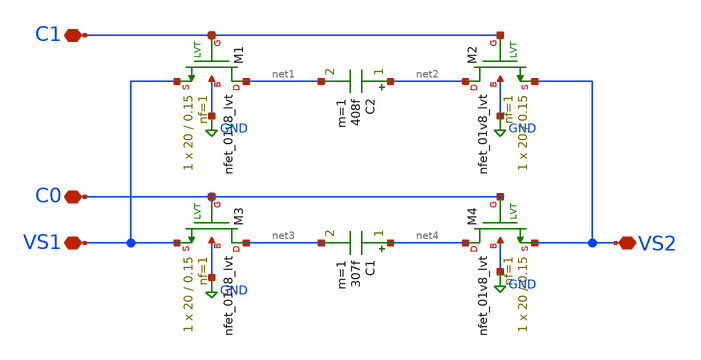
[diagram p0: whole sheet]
** sch_path: VGA/Cs_Banks.sch
**.subckt Cs_Banks VS1 VS2 C0 C1
*.iopin VS1
*.iopin VS2
*.iopin C0
*.iopin C1
XM1 net1 C1 VS1 GND sky130_fd_pr__nfet_01v8_lvt L=0.15 W=20 nf=1 ad='int((1 + 1)/2) * 20 / 1 * 0.29'
+ as='int((1 + 2)/2) * 20 / 1 * 0.29' pd='2*int((1 + 1)/2) * (20 / 1 + 0.29)' ps='2*int((1 + 2)/2) * (20 / 1 + 0.29)'
+ nrd='0.29 / 20 ' nrs='0.29 / 20 ' sa=0 sb=0 sd=0 mult=1 m=1
XM3 net3 C0 VS1 GND sky130_fd_pr__nfet_01v8_lvt L=0.15 W=20 nf=1 ad='int((1 + 1)/2) * 20 / 1 * 0.29'
+ as='int((1 + 2)/2) * 20 / 1 * 0.29' pd='2*int((1 + 1)/2) * (20 / 1 + 0.29)' ps='2*int((1 + 2)/2) * (20 / 1 + 0.29)'
+ nrd='0.29 / 20 ' nrs='0.29 / 20 ' sa=0 sb=0 sd=0 mult=1 m=1
C2 net2 net1 408f m=1
C1 net4 net3 307f m=1
XM2 net2 C1 VS2 GND sky130_fd_pr__nfet_01v8_lvt L=0.15 W=20 nf=1 ad='int((1 + 1)/2) * 20 / 1 * 0.29'
+ as='int((1 + 2)/2) * 20 / 1 * 0.29' pd='2*int((1 + 1)/2) * (20 / 1 + 0.29)' ps='2*int((1 + 2)/2) * (20 / 1 + 0.29)'
+ nrd='0.29 / 20 ' nrs='0.29 / 20 ' sa=0 sb=0 sd=0 mult=1 m=1
XM4 net4 C0 VS2 GND sky130_fd_pr__nfet_01v8_lvt L=0.15 W=20 nf=1 ad='int((1 + 1)/2) * 20 / 1 * 0.29'
+ as='int((1 + 2)/2) * 20 / 1 * 0.29' pd='2*int((1 + 1)/2) * (20 / 1 + 0.29)' ps='2*int((1 + 2)/2) * (20 / 1 + 0.29)'
+ nrd='0.29 / 20 ' nrs='0.29 / 20 ' sa=0 sb=0 sd=0 mult=1 m=1
**.ends
.GLOBAL GND
.end
